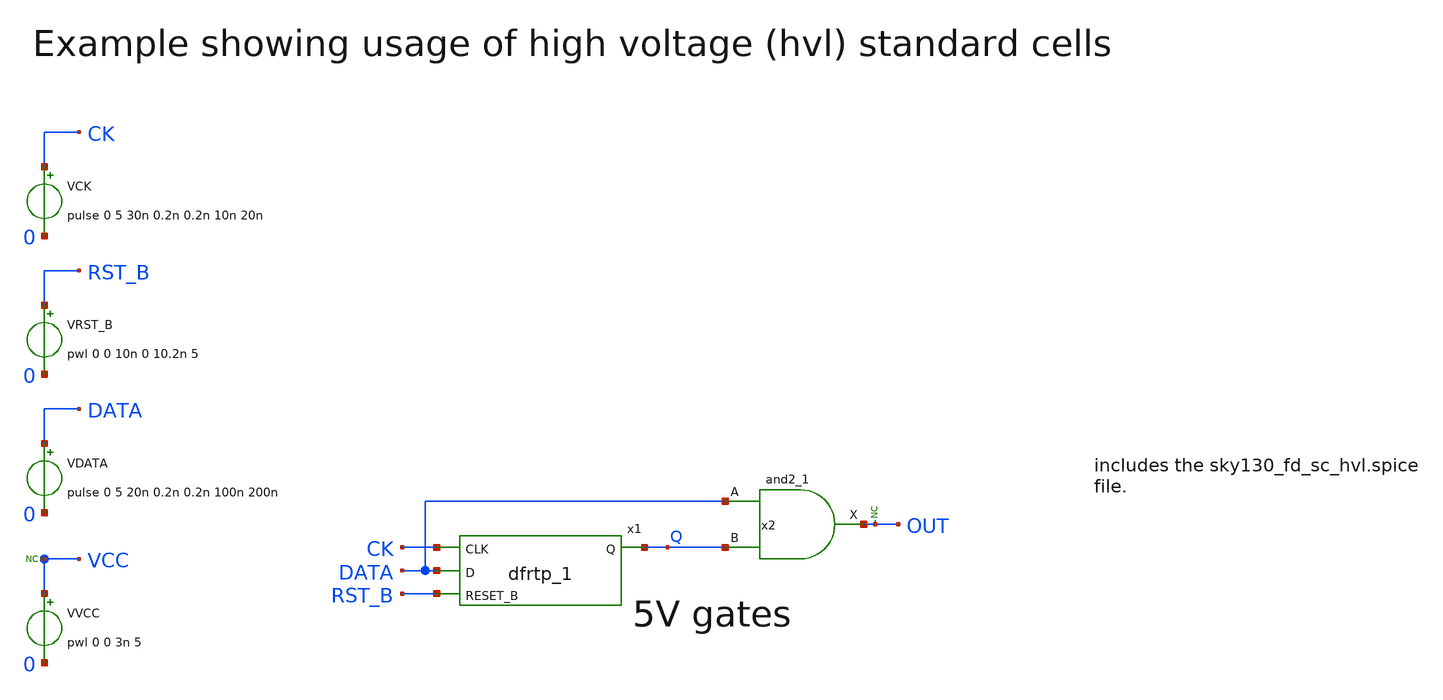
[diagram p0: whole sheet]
** sch_path: sky130A/xschem_libs/sky130_tests_ase/test_hvl_cells/schematic/test_hvl_cells.sch
* Copyright 2021 Stefan Frederik Schippers
* Licensed under the Apache License, Version 2.0 (the "License");
* you may not use this file except in compliance with the License.
* You may obtain a copy of the License at
* https://www.apache.org/licenses/LICENSE-2.0
* Unless required by applicable law or agreed to in writing, software
* distributed under the License is distributed on an "AS IS" BASIS,
* WITHOUT WARRANTIES OR CONDITIONS OF ANY KIND, either express or implied.
* See the License for the specific language governing permissions and
* limitations under the License.
**.subckt test_hvl_cells
VVCC VCC 0 pwl 0 0 3n 5
x1 CK DATA RST_B 0 0 VCC VCC Q sky130_fd_sc_hvl__dfrtp_1
x2 DATA Q 0 0 VCC VCC OUT sky130_fd_sc_hvl__and2_1
VCK CK 0 pulse 0 5 30n 0.2n 0.2n 10n 20n
VDATA DATA 0 pulse 0 5 20n 0.2n 0.2n 100n 200n
VRST_B RST_B 0 pwl 0 0 10n 0 10.2n 5
* noconn VCC
* noconn OUT
**.ends
.end
